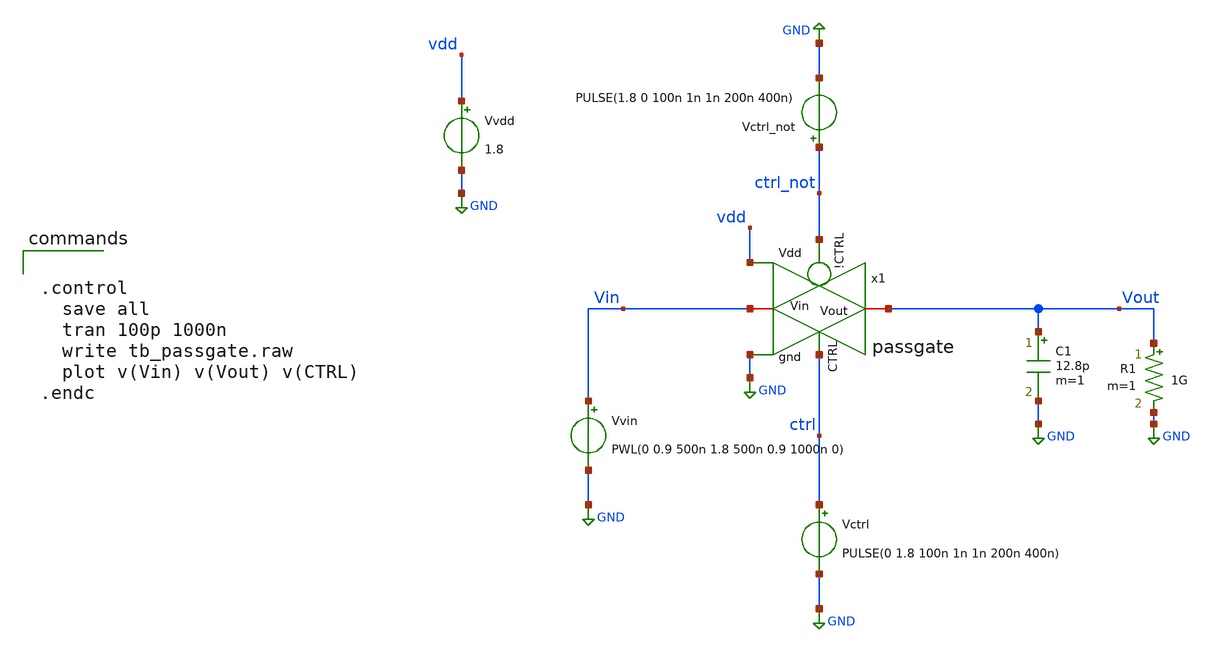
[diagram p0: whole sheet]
** sch_path: 05_mixed_signal/soluzioni/lab01/xschem/tb_passgate.sch
**.subckt tb_passgate
Vvdd vdd GND 1.8
x1 Vin GND ctrl_not ctrl vdd Vout passgate
Vvin Vin GND PWL(0 0.9 500n 1.8 500n 0.9 1000n 0)
Vctrl ctrl GND PULSE(0 1.8 100n 1n 1n 200n 400n)
Vctrl_not ctrl_not GND PULSE(1.8 0 100n 1n 1n 200n 400n)
C1 Vout GND 12.8p m=1
R1 Vout GND 1G m=1
**** begin user architecture code


.control
  save all
  tran 100p 1000n
  write tb_passgate.raw
  plot v(Vin) v(Vout) v(CTRL)
.endc



** opencircuitdesign pdks install
.lib $::SKYWATER_MODELS/sky130.lib.spice tt

**** end user architecture code
**.ends

* expanding   symbol:  passgate.sym # of pins=6
** sym_path: 05_mixed_signal/soluzioni/lab03/xschem/passgate.sym
** sch_path: 05_mixed_signal/soluzioni/lab03/xschem/passgate.sch
.subckt passgate Vin gnd !CTRL CTRL Vdd Vout
*.ipin CTRL
*.ipin !CTRL
*.iopin Vin
*.iopin Vout
*.ipin Vdd
*.ipin gnd
XM3 Vin CTRL Vout gnd sky130_fd_pr__nfet_01v8_lvt L=0.15 W=6 nf=1 ad='int((1 + 1)/2) * 6 / 1 * 0.29'
+ as='int((1 + 2)/2) * 6 / 1 * 0.29' pd='2*int((1 + 1)/2) * (6 / 1 + 0.29)' ps='2*int((1 + 2)/2) * (6 / 1 + 0.29)'
+ nrd='0.29 / 6 ' nrs='0.29 / 6 ' sa=0 sb=0 sd=0 mult=1 m=1
XM1 Vin !CTRL Vout Vdd sky130_fd_pr__pfet_01v8_lvt L=0.35 W=12 nf=1 ad='int((1 + 1)/2) * 12 / 1 * 0.29'
+ as='int((1 + 2)/2) * 12 / 1 * 0.29' pd='2*int((1 + 1)/2) * (12 / 1 + 0.29)' ps='2*int((1 + 2)/2) * (12 / 1 + 0.29)'
+ nrd='0.29 / 12 ' nrs='0.29 / 12 ' sa=0 sb=0 sd=0 mult=1 m=1
.ends

.GLOBAL GND
.end
